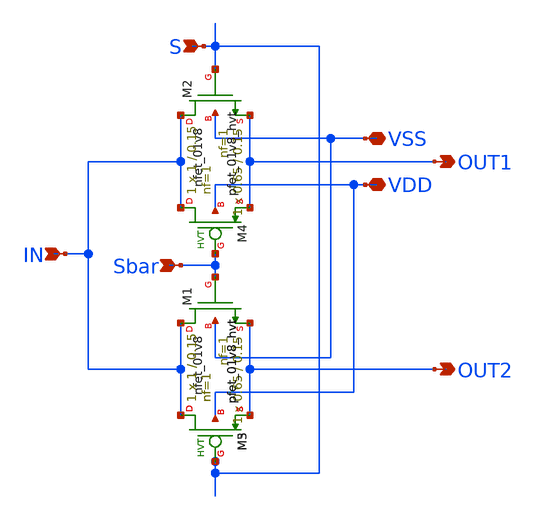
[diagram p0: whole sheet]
** sch_path: xiaolin/demux2-1.sch
**.subckt demux2-1 Sbar S VSS VDD OUT1 OUT2 IN
*.ipin Sbar
*.ipin S
*.iopin VSS
*.iopin VDD
*.opin OUT1
*.opin OUT2
*.ipin IN
XM2 IN S OUT1 VSS sky130_fd_pr__nfet_01v8 L=0.15 W=0.65 nf=1 ad='int((nf+1)/2) * W/nf * 0.29' as='int((nf+2)/2) * W/nf * 0.29'
+ pd='2*int((nf+1)/2) * (W/nf + 0.29)' ps='2*int((nf+2)/2) * (W/nf + 0.29)' nrd='0.29 / W' nrs='0.29 / W'
+ sa=0 sb=0 sd=0 mult=1 m=1
XM1 IN Sbar OUT2 VSS sky130_fd_pr__nfet_01v8 L=0.15 W=0.65 nf=1 ad='int((nf+1)/2) * W/nf * 0.29' as='int((nf+2)/2) * W/nf * 0.29'
+ pd='2*int((nf+1)/2) * (W/nf + 0.29)' ps='2*int((nf+2)/2) * (W/nf + 0.29)' nrd='0.29 / W' nrs='0.29 / W'
+ sa=0 sb=0 sd=0 mult=1 m=1
XM3 IN S OUT2 VDD sky130_fd_pr__pfet_01v8_hvt L=0.15 W=1 nf=1 ad='int((nf+1)/2) * W/nf * 0.29' as='int((nf+2)/2) * W/nf * 0.29'
+ pd='2*int((nf+1)/2) * (W/nf + 0.29)' ps='2*int((nf+2)/2) * (W/nf + 0.29)' nrd='0.29 / W' nrs='0.29 / W'
+ sa=0 sb=0 sd=0 mult=1 m=1
XM4 IN Sbar OUT1 VDD sky130_fd_pr__pfet_01v8_hvt L=0.15 W=1 nf=1 ad='int((nf+1)/2) * W/nf * 0.29' as='int((nf+2)/2) * W/nf * 0.29'
+ pd='2*int((nf+1)/2) * (W/nf + 0.29)' ps='2*int((nf+2)/2) * (W/nf + 0.29)' nrd='0.29 / W' nrs='0.29 / W'
+ sa=0 sb=0 sd=0 mult=1 m=1
XM5 IN S OUT2 VDD sky130_fd_pr__pfet_01v8_hvt L=0.15 W=1 nf=1 ad='int((nf+1)/2) * W/nf * 0.29' as='int((nf+2)/2) * W/nf * 0.29'
+ pd='2*int((nf+1)/2) * (W/nf + 0.29)' ps='2*int((nf+2)/2) * (W/nf + 0.29)' nrd='0.29 / W' nrs='0.29 / W'
+ sa=0 sb=0 sd=0 mult=1 m=1
**.ends
.end
